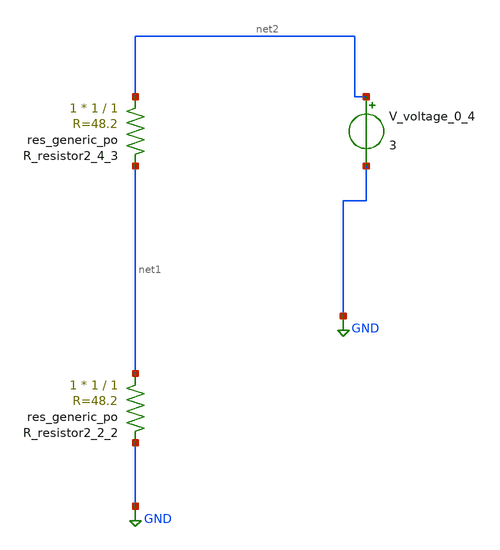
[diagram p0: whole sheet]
** sch_path: schematics/AMSNet/649.sch
**.subckt 649
XR_resistor2_2_2 net1 GND sky130_fd_pr__res_generic_po W=1 L=1 m=1
XR_resistor2_4_3 net2 net1 sky130_fd_pr__res_generic_po W=1 L=1 m=1
V_voltage_0_4 net2 GND 3
**.ends
.GLOBAL GND
.end
